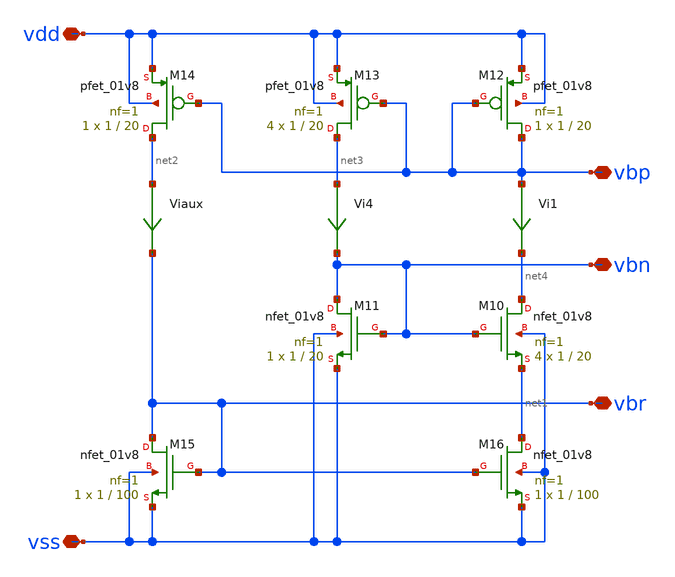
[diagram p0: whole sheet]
** sch_path: playground/OgueyAebischerBias.sch
**.subckt OgueyAebischerBias vss vdd vbp vbn vbr
*.iopin vss
*.iopin vdd
*.iopin vbp
*.iopin vbn
*.iopin vbr
XM10 net4 vbn net1 vss sky130_fd_pr__nfet_01v8 L=20 W=1 nf=1 ad='int((1 + 1)/2) * 1 / 1 * 0.29' as='int((1 + 2)/2) * 1 / 1 * 0.29'
+ pd='2*int((1 + 1)/2) * (1 / 1 + 0.29)' ps='2*int((1 + 2)/2) * (1 / 1 + 0.29)' nrd='0.29 / 1 ' nrs='0.29 / 1 '
+ sa=0 sb=0 sd=0 mult=4 m=4
XM12 vbp vbp vdd vdd sky130_fd_pr__pfet_01v8 L=20 W=1 nf=1 ad='int((nf+1)/2) * W/nf * 0.29' as='int((nf+2)/2) * W/nf * 0.29'
+ pd='2*int((nf+1)/2) * (W/nf + 0.29)' ps='2*int((nf+2)/2) * (W/nf + 0.29)' nrd='0.29 / W' nrs='0.29 / W'
+ sa=0 sb=0 sd=0 mult=1 m=1
XM11 vbn vbn vss vss sky130_fd_pr__nfet_01v8 L=20 W=1 nf=1 ad='int((1 + 1)/2) * 1 / 1 * 0.29' as='int((1 + 2)/2) * 1 / 1 * 0.29'
+ pd='2*int((1 + 1)/2) * (1 / 1 + 0.29)' ps='2*int((1 + 2)/2) * (1 / 1 + 0.29)' nrd='0.29 / 1 ' nrs='0.29 / 1 '
+ sa=0 sb=0 sd=0 mult=1 m=1
XM13 net3 vbp vdd vdd sky130_fd_pr__pfet_01v8 L=20 W=1 nf=1 ad='int((nf+1)/2) * W/nf * 0.29' as='int((nf+2)/2) * W/nf * 0.29'
+ pd='2*int((nf+1)/2) * (W/nf + 0.29)' ps='2*int((nf+2)/2) * (W/nf + 0.29)' nrd='0.29 / W' nrs='0.29 / W'
+ sa=0 sb=0 sd=0 mult=4 m=4
XM14 net2 vbp vdd vdd sky130_fd_pr__pfet_01v8 L=20 W=1 nf=1 ad='int((nf+1)/2) * W/nf * 0.29' as='int((nf+2)/2) * W/nf * 0.29'
+ pd='2*int((nf+1)/2) * (W/nf + 0.29)' ps='2*int((nf+2)/2) * (W/nf + 0.29)' nrd='0.29 / W' nrs='0.29 / W'
+ sa=0 sb=0 sd=0 mult=1 m=1
XM16 net1 vbr vss vss sky130_fd_pr__nfet_01v8 L=100 W=1 nf=1 ad='int((1 + 1)/2) * 1 / 1 * 0.29' as='int((1 + 2)/2) * 1 / 1 * 0.29'
+ pd='2*int((1 + 1)/2) * (1 / 1 + 0.29)' ps='2*int((1 + 2)/2) * (1 / 1 + 0.29)' nrd='0.29 / 1 ' nrs='0.29 / 1 '
+ sa=0 sb=0 sd=0 mult=1 m=1
XM15 vbr vbr vss vss sky130_fd_pr__nfet_01v8 L=100 W=1 nf=1 ad='int((1 + 1)/2) * 1 / 1 * 0.29' as='int((1 + 2)/2) * 1 / 1 * 0.29'
+ pd='2*int((1 + 1)/2) * (1 / 1 + 0.29)' ps='2*int((1 + 2)/2) * (1 / 1 + 0.29)' nrd='0.29 / 1 ' nrs='0.29 / 1 '
+ sa=0 sb=0 sd=0 mult=1 m=1
Vi1 vbp net4 0
.save i(vi1)
Vi4 net3 vbn 0
.save i(vi4)
Viaux net2 vbr 0
.save i(viaux)
**.ends
.end
